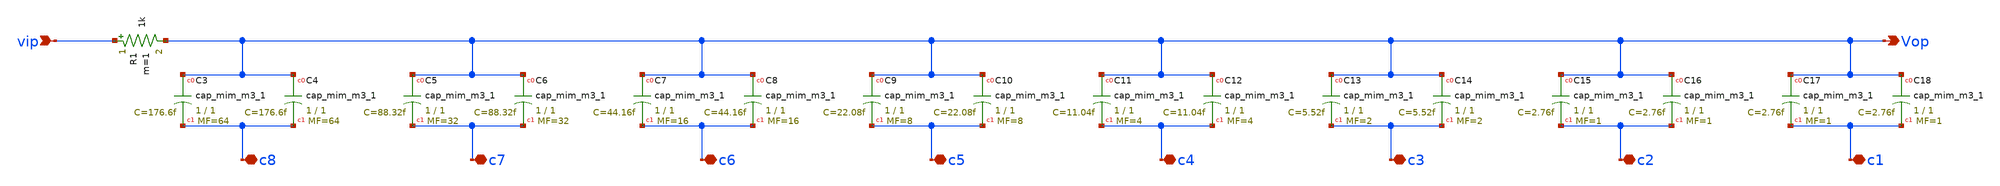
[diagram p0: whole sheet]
** sch_path: sar-adc/updated/C_DAC.sch
**.subckt C_DAC Vop vip c8 c7 c6 c5 c4 c3 c2 c1
*.opin Vop
*.ipin vip
*.iopin c8
*.iopin c7
*.iopin c6
*.iopin c5
*.iopin c4
*.iopin c3
*.iopin c2
*.iopin c1
XC3 Vop c8 sky130_fd_pr__cap_mim_m3_1 W=1 L=1 MF=64 m=64
XC4 Vop c8 sky130_fd_pr__cap_mim_m3_1 W=1 L=1 MF=64 m=64
XC5 Vop c7 sky130_fd_pr__cap_mim_m3_1 W=1 L=1 MF=32 m=32
XC6 Vop c7 sky130_fd_pr__cap_mim_m3_1 W=1 L=1 MF=32 m=32
XC7 Vop c6 sky130_fd_pr__cap_mim_m3_1 W=1 L=1 MF=16 m=16
XC8 Vop c6 sky130_fd_pr__cap_mim_m3_1 W=1 L=1 MF=16 m=16
XC9 Vop c5 sky130_fd_pr__cap_mim_m3_1 W=1 L=1 MF=8 m=8
XC10 Vop c5 sky130_fd_pr__cap_mim_m3_1 W=1 L=1 MF=8 m=8
XC11 Vop c4 sky130_fd_pr__cap_mim_m3_1 W=1 L=1 MF=4 m=4
XC12 Vop c4 sky130_fd_pr__cap_mim_m3_1 W=1 L=1 MF=4 m=4
XC13 Vop c3 sky130_fd_pr__cap_mim_m3_1 W=1 L=1 MF=2 m=2
XC14 Vop c3 sky130_fd_pr__cap_mim_m3_1 W=1 L=1 MF=2 m=2
XC15 Vop c2 sky130_fd_pr__cap_mim_m3_1 W=1 L=1 MF=1 m=1
XC16 Vop c2 sky130_fd_pr__cap_mim_m3_1 W=1 L=1 MF=1 m=1
XC17 Vop c1 sky130_fd_pr__cap_mim_m3_1 W=1 L=1 MF=1 m=1
XC18 Vop c1 sky130_fd_pr__cap_mim_m3_1 W=1 L=1 MF=1 m=1
R1 vip Vop 1k m=1
**.ends
.end
